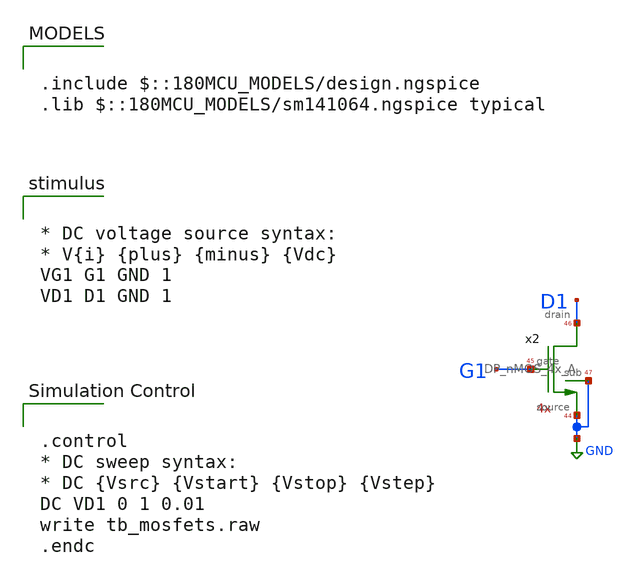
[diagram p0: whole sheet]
** sch_path: designs/libs/tb_MOSbius_v1/tb_mosfets/tb_mosfets.sch
**.subckt tb_mosfets
x2 D1 GND G1 GND DP_nMOS_4x_A
**** begin user architecture code


* DC voltage source syntax:
* V{i} {plus} {minus} {Vdc}
VG1 G1 GND 1
VD1 D1 GND 1




.control
* DC sweep syntax:
* DC {Vsrc} {Vstart} {Vstop} {Vstep}
DC VD1 0 1 0.01
write tb_mosfets.raw
.endc



.include $::180MCU_MODELS/design.ngspice
.lib $::180MCU_MODELS/sm141064.ngspice typical

**** end user architecture code
**.ends

* expanding   symbol:  libs/MOSbius_v1/DP_nMOS_4x_A/DP_nMOS_4x_A.sym # of pins=4
** sym_path: designs/libs/MOSbius_v1/DP_nMOS_4x_A/DP_nMOS_4x_A.sym
** sch_path: designs/libs/MOSbius_v1/DP_nMOS_4x_A/DP_nMOS_4x_A.sch
.subckt DP_nMOS_4x_A drain sub gate source
*.iopin drain
*.iopin source
*.iopin sub
*.iopin gate
XM1 drain gate source sub nfet_03v3 L=0.5u W=4u nf=2 ad='int((nf+1)/2) * W/nf * 0.18u' as='int((nf+2)/2) * W/nf * 0.18u'
+ pd='2*int((nf+1)/2) * (W/nf + 0.18u)' ps='2*int((nf+2)/2) * (W/nf + 0.18u)' nrd='0.18u / W' nrs='0.18u / W'
+ sa=0 sb=0 sd=0 m=1
.ends

.GLOBAL GND
.end
